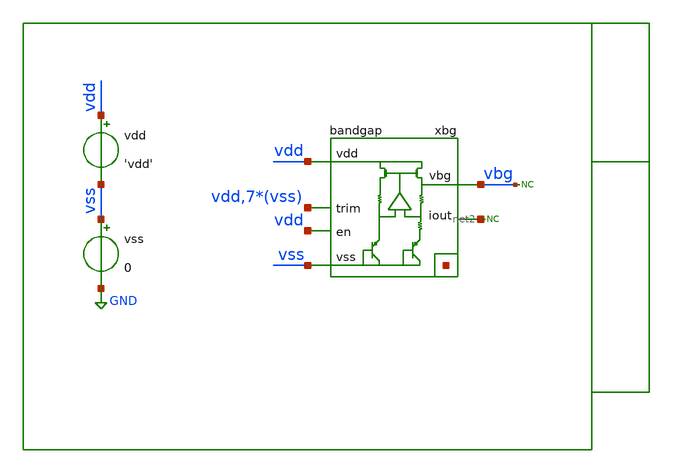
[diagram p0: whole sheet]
** sch_path: xschem/tb/bandgap_cm/bandgap/dc_bandgap_supply.sch
**.subckt dc_bandgap_supply
xbg vdd vbg vss net1[7] net1[6] net1[5] net1[4] net1[3] net1[2] net1[1] net1[0] vdd vss vss vss vss
+ vss vss vss net2 vdd bandgap
vdd vdd vss 'vdd'
vss vss GND 0
* noconn vbg
* noconn #net2
**** begin user architecture code

* Control

.param vdd = 3.3
.temp 27

.options reltol     = 1e-6

*------------------------------------------------------------
* Nodeset for better convergence
*------------------------------------------------------------
* .nodeset v(vbg)  = '1'
* .nodeset v(xbg.gate) = 'vdd/2'
* .nodeset v(xbg.vx)   = '0.70'
* .nodeset v(xbg.vbe2) = '0.65'
* .nodeset v(xbg.vs1)  = '0'
*------------------------------------------------------------

*------------------------------------------------------------
* Save device current for DC analysis
*------------------------------------------------------------
.save @m.xbg.xm1.m0[id]
.save @m.xbg.xm2.m0[id]
.save @m.xbg.xmb3.m0[id]

.control
save all

*optran 0 0 0 100n 0.1m 0

dc vdd  2.5 5 0.1

let id_xm1 = @m.xbg.xm1.m0[id]
let id_xm2 = @m.xbg.xm2.m0[id]
let ibias = @m.xbg.xmb3.m0[id]

let ic_ratio = id_xm1/id_xm2

gnuplot p1 vbg

meas dc vbg_min min vbg from=2.5 to=5
meas dc vbg_max max vbg from=2.5 to=5

let dv_dvdd = (vbg_max-vbg_min)/(5-2.5)

print vbg_min
print vbg_max
print dv_dvdd

gnuplot p2 ibias
.endc
.end


 * Model Corners

.include $::CORNERS/ngspice/tt.spice
*.include $::CORNERS/ngspice/ff.spice
*.include $::CORNERS/ngspice/ss.spice
*.include $::CORNERS/ngspice/sf.spice
*.include $::CORNERS/ngspice/fs.spice

**** end user architecture code
**.ends
.GLOBAL GND
.end
